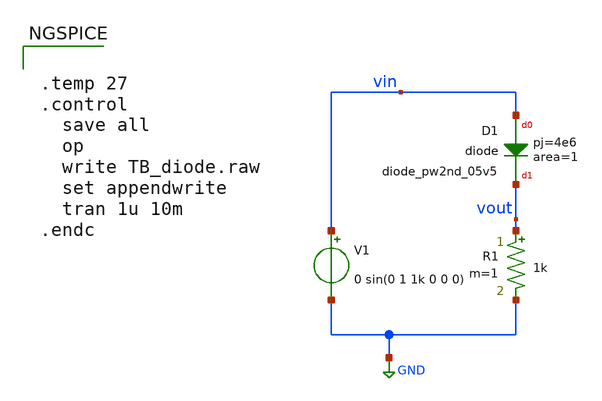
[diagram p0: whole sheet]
** sch_path: xschem/TB_diode.sch
**.subckt TB_diode
R1 vout GND 1k m=1
V1 vin GND 0 sin(0 1 1k 0 0 0)
XD1 vin vout sky130_fd_pr__diode_pw2nd_05v5 area=1 pj=4e6
**** begin user architecture code

** opencircuitdesign pdks install
.lib $::SKYWATER_MODELS/sky130.lib.spice tt



.temp 27
.control
  save all
  op
  write TB_diode.raw
  set appendwrite
  tran 1u 10m
.endc


**** end user architecture code
**.ends
.GLOBAL GND
.end
